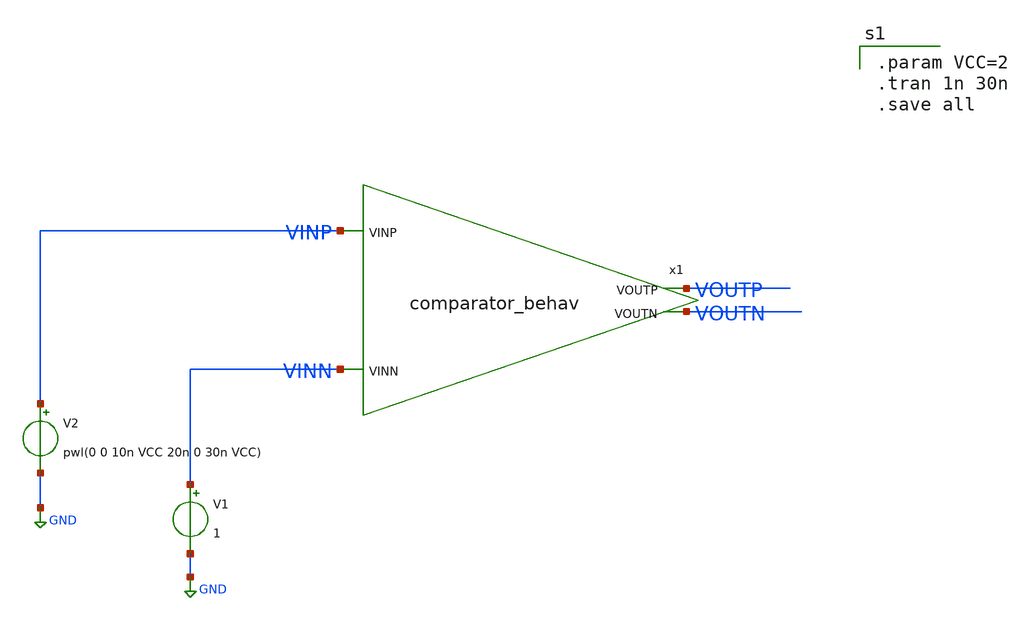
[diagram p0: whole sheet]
** sch_path: comparator_tb.sch
**.subckt comparator_tb
V1 VINN GND 1
V2 VINP GND pwl(0 0 10n VCC 20n 0 30n VCC)
x1 VOUTP VINP VINN VOUTN comparator_behav
**** begin user architecture code

.param VCC=2
.tran 1n 30n
.save all


**** end user architecture code
**.ends

* expanding   symbol:  comparator_behav.sym # of pins=4
** sym_path: comparator_behav.sym
** sch_path: comparator_behav.sch
.subckt comparator_behav VOUTP VINP VINN VOUTN
*.ipin VINP
*.ipin VINN
*.opin VOUTP
*.opin VOUTN
V1 VINPi VINP 0
V2 VINNi VINN 0
B1 VOUTP GND V = {VCC/2 + VCC/2*(tanh(V(VINPi,VINNi)*1e6))}
B2 VOUTN GND V = {VCC/2 + VCC/2*(tanh(V(VINPi,VINNi)*1e6*-1))}
.ends

.GLOBAL GND
.end
